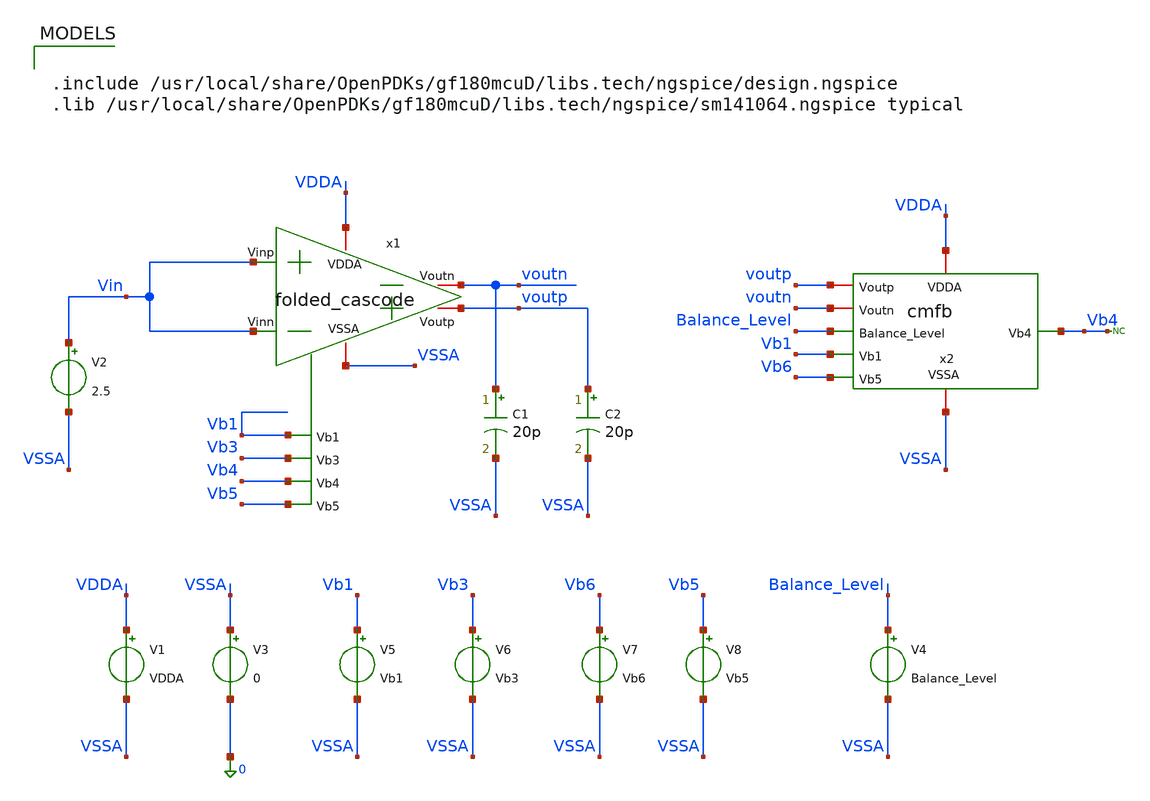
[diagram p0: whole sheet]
** sch_path: Folded_cascode/testbenches/simulation/fc_cmfb_op_tb_batch.sch
**.subckt fc_cmfb_op_tb_batch
x1 VDDA VSSA Vin Vin voutp voutn Vb1 Vb3 Vb4 Vb5 folded_cascode
x2 VDDA VSSA voutp voutn Balance_Level Vb1 Vb4 Vb6 cmfb
V2 Vin VSSA 2.5
C1 voutn VSSA 20p m=1
C2 voutp VSSA 20p m=1
V1 VDDA VSSA VDDA
V3 VSSA 0 0
V5 Vb1 VSSA Vb1
V6 Vb3 VSSA Vb3
V8 Vb5 VSSA Vb5
V4 Balance_Level VSSA Balance_Level
V7 Vb6 VSSA Vb6
* noconn Vb4
**** begin user architecture code

.include /usr/local/share/OpenPDKs/gf180mcuD/libs.tech/ngspice/design.ngspice
.lib /usr/local/share/OpenPDKs/gf180mcuD/libs.tech/ngspice/sm141064.ngspice typical



.temp 27
.param VDDA = 5
.param Balance_Level = 1.3
.param Vb1 = 3.96
.param Vb3 = 3.6
.param Vb5 = 0.72
.param Vb6 = 0.83

.param VD = 0

.control
option sparse
set filetype=ascii
set wr_singlescale
set wr_vecnames
save all
save @m.x1.xm1.m0[id]
save @m.x1.xm1.m0[gm]
save @m.x1.xm1.m0[vgs]
save @m.x1.xm1.m0[vds]
save @m.x1.xm1.m0[vth]
save @m.x1.xm1.m0[gds]

save @m.x1.xm2.m0[id]
save @m.x1.xm2.m0[gm]
save @m.x1.xm2.m0[vgs]
save @m.x1.xm2.m0[vds]
save @m.x1.xm2.m0[vth]
save @m.x1.xm2.m0[gds]

save @m.x1.xm9.m0[id]
save @m.x1.xm9.m0[gm]
save @m.x1.xm9.m0[vgs]
save @m.x1.xm9.m0[vds]
save @m.x1.xm9.m0[vth]
save @m.x1.xm9.m0[gds]

save @m.x1.xm8.m0[id]
save @m.x1.xm8.m0[gm]
save @m.x1.xm8.m0[vgs]
save @m.x1.xm8.m0[vds]
save @m.x1.xm8.m0[vth]
save @m.x1.xm8.m0[gds]

save @m.x1.xm6.m0[id]
save @m.x1.xm6.m0[gm]
save @m.x1.xm6.m0[vgs]
save @m.x1.xm6.m0[vds]
save @m.x1.xm6.m0[vth]
save @m.x1.xm6.m0[gds]

save @m.x1.xm5.m0[id]
save @m.x1.xm5.m0[gm]
save @m.x1.xm5.m0[vgs]
save @m.x1.xm5.m0[vds]
save @m.x1.xm5.m0[vth]
save @m.x1.xm5.m0[gds]
save @m.x1.xm5.m0[vdsat]
save @m.x1.xm4.m0[vdsat]

save @m.x2.xm1.m0[id]
save @m.x2.xm1.m0[gm]
save @m.x2.xm1.m0[vgs]
save @m.x2.xm1.m0[vds]
save @m.x2.xm1.m0[vth]
save @m.x2.xm1.m0[gds]

save @m.x2.xm2.m0[id]
save @m.x2.xm2.m0[gm]
save @m.x2.xm2.m0[vgs]
save @m.x2.xm2.m0[vds]
save @m.x2.xm2.m0[vth]
save @m.x2.xm2.m0[gds]

save @m.x2.xm3.m0[id]
save @m.x2.xm3.m0[gm]
save @m.x2.xm3.m0[vgs]
save @m.x2.xm3.m0[vds]
save @m.x2.xm3.m0[vth]
save @m.x2.xm3.m0[gds]

save @m.x2.xm4.m0[id]
save @m.x2.xm4.m0[gm]
save @m.x2.xm4.m0[vgs]
save @m.x2.xm4.m0[vds]
save @m.x2.xm4.m0[vth]
save @m.x2.xm4.m0[gds]

save @m.x2.xm5.m0[id]
save @m.x2.xm5.m0[gm]
save @m.x2.xm5.m0[vgs]
save @m.x2.xm5.m0[vds]
save @m.x2.xm5.m0[vth]
save @m.x2.xm5.m0[gds]

save @m.x2.xm6.m0[id]
save @m.x2.xm6.m0[gm]
save @m.x2.xm6.m0[vgs]
save @m.x2.xm6.m0[vds]
save @m.x2.xm6.m0[vth]
save @m.x2.xm6.m0[gds]

save @m.x2.xm7.m0[id]
save @m.x2.xm7.m0[gm]
save @m.x2.xm7.m0[vgs]
save @m.x2.xm7.m0[vds]
save @m.x2.xm7.m0[vth]
save @m.x2.xm7.m0[gds]

save @m.x2.xm8.m0[id]
save @m.x2.xm8.m0[gm]
save @m.x2.xm8.m0[vgs]
save @m.x2.xm8.m0[vds]
save @m.x2.xm8.m0[vth]
save @m.x2.xm8.m0[gds]

save @m.x2.xm9.m0[id]
save @m.x2.xm9.m0[gm]
save @m.x2.xm9.m0[vgs]
save @m.x2.xm9.m0[vds]
save @m.x2.xm9.m0[vth]
save @m.x2.xm9.m0[gds]

op
*dc V7 0.80 1.50 0.002

*let vcm_out = (v(Voutp)+v(Voutn))/2
*let gmid_m5 = @m.x1.xm5.m0[gm]/@m.x1.xm5.m0[id]
*let satmargin_m5 = @m.x1.xm5.m0[vds]-@m.x1.xm5.m0[vdsat]

*print v(Voutp) v(Voutn) vcm_out
*print @m.x1.xm5.m0[id]
*print @m.x1.xm5.m0[gm]
*print gmid_m5
*print @m.x1.xm5.m0[vgs]
*print @m.x1.xm5.m0[vds]
*print @m.x1.xm5.m0[vdsat]
*print satmargin_m5

*wrdata fc_vb4_results.txt v(Voutp) v(Voutn) vcm_out @m.x1.xm5.m0[id] @m.x1.xm5.m0[gm] gmid_m5
*+ @m.x1.xm5.m0[vds] @m.x1.xm5.m0[vdsat] satmargin_m5

write fc_cmfb_op_tb.raw

.endc


**** end user architecture code
**.ends
.end
